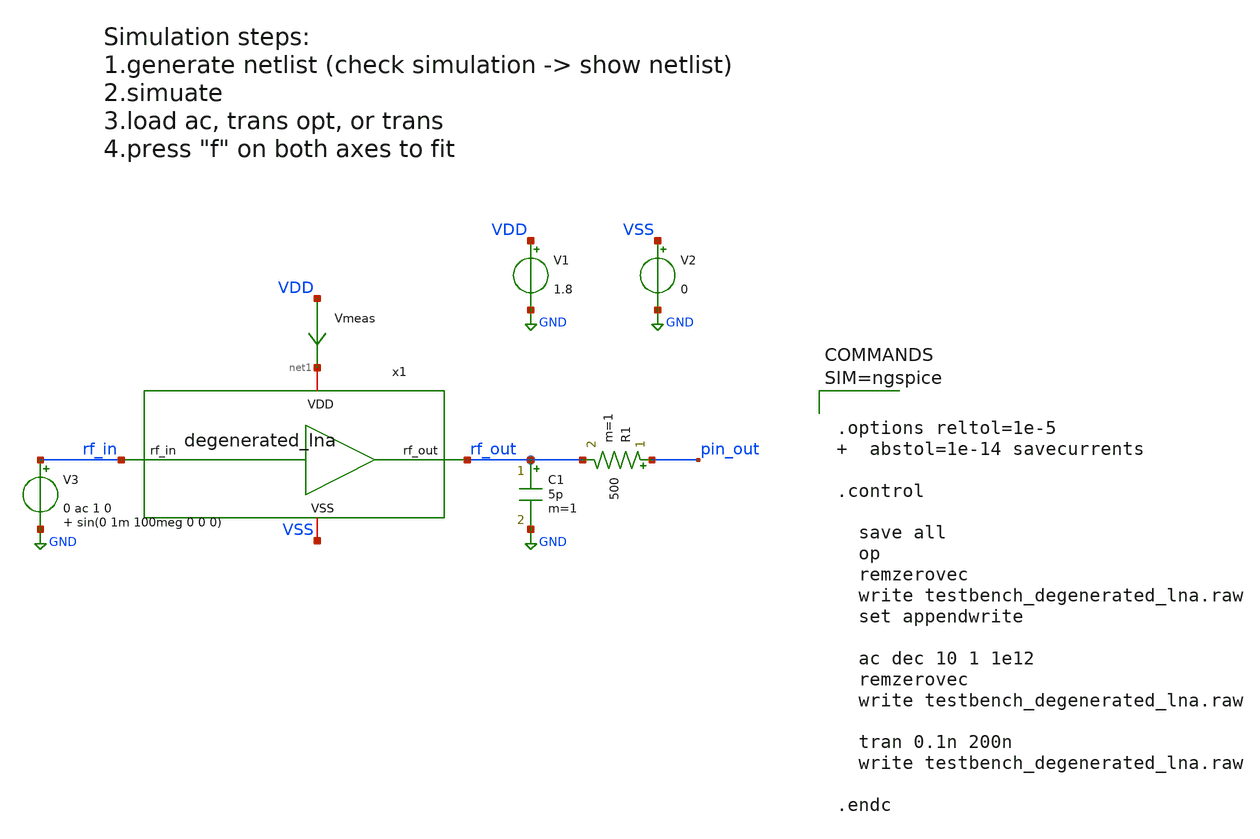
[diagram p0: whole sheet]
** sch_path: xschem/testbench_degenerated_lna.sch
**.subckt testbench_degenerated_lna
x1 net1 VSS rf_out rf_in degenerated_lna
V1 VDD GND 1.8
V2 VSS GND 0
R1 pin_out rf_out 500 m=1
C1 rf_out GND 5p m=1
V3 rf_in GND 0 ac 1 0 sin(0 1m 100meg 0 0 0)
Vmeas VDD net1 0
.save i(vmeas)
**** begin user architecture code

** opencircuitdesign pdks install
.lib $::SKYWATER_MODELS/sky130.lib.spice tt





.options reltol=1e-5   abstol=1e-14 savecurrents

.control

  save all
  op
  remzerovec
  write testbench_degenerated_lna.raw
  set appendwrite

  ac dec 10 1 1e12
  remzerovec
  write testbench_degenerated_lna.raw

  tran 0.1n 200n
  write testbench_degenerated_lna.raw

.endc



**** end user architecture code
**.ends

* expanding   symbol:  degenerated_lna.sym # of pins=4
** sym_path: xschem/degenerated_lna.sym
** sch_path: xschem/degenerated_lna.sch
.subckt degenerated_lna VDD VSS rf_out rf_in
*.iopin VDD
*.iopin VSS
*.ipin rf_in
*.opin rf_out
XM1 net1 net1 VSS VSS sky130_fd_pr__nfet_01v8 L=0.15 W=10 nf=1 ad='int((nf+1)/2) * W/nf * 0.29' as='int((nf+2)/2) * W/nf * 0.29'
+ pd='2*int((nf+1)/2) * (W/nf + 0.29)' ps='2*int((nf+2)/2) * (W/nf + 0.29)' nrd='0.29 / W' nrs='0.29 / W'
+ sa=0 sb=0 sd=0 mult=1 m=1
XM2 Vds Vgs VSS VSS sky130_fd_pr__nfet_01v8 L=0.15 W=10 nf=1 ad='int((nf+1)/2) * W/nf * 0.29' as='int((nf+2)/2) * W/nf * 0.29'
+ pd='2*int((nf+1)/2) * (W/nf + 0.29)' ps='2*int((nf+2)/2) * (W/nf + 0.29)' nrd='0.29 / W' nrs='0.29 / W'
+ sa=0 sb=0 sd=0 mult=1 m=1
XC1 Vgs rf_in sky130_fd_pr__cap_mim_m3_1 W=30 L=30 MF=1 m=1
XC2 rf_out Vds sky130_fd_pr__cap_mim_m3_1 W=30 L=30 MF=1 m=1
XR1 Vgs net1 net2 sky130_fd_pr__res_xhigh_po_0p35 L=4 mult=1 m=1
XR2 net1 VDD net3 sky130_fd_pr__res_high_po_0p69 L=3.45 mult=1 m=1
XR3 Vds VDD net4 sky130_fd_pr__res_high_po_0p69 L=3.45 mult=1 m=1
.ends

.GLOBAL GND
.end
